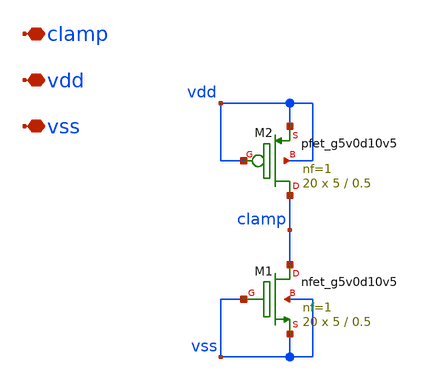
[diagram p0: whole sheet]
** sch_path: images/iic-osic-tools/addons/examples/Open-PMIC-tapeout/xschem/esd_clamp_well.sch
**.subckt esd_clamp_well clamp vdd vss
*.iopin clamp
*.iopin vdd
*.iopin vss
XM1 clamp vss vss vss sky130_fd_pr__nfet_g5v0d10v5 L=0.5 W=5 nf=1 ad='int((nf+1)/2) * W/nf * 0.29' as='int((nf+2)/2) * W/nf * 0.29'
+ pd='2*int((nf+1)/2) * (W/nf + 0.29)' ps='2*int((nf+2)/2) * (W/nf + 0.29)' nrd='0.29 / W' nrs='0.29 / W'
+ sa=0 sb=0 sd=0 mult=20 m=20
XM2 clamp vdd vdd vdd sky130_fd_pr__pfet_g5v0d10v5 L=0.5 W=5 nf=1 ad='int((nf+1)/2) * W/nf * 0.29' as='int((nf+2)/2) * W/nf * 0.29'
+ pd='2*int((nf+1)/2) * (W/nf + 0.29)' ps='2*int((nf+2)/2) * (W/nf + 0.29)' nrd='0.29 / W' nrs='0.29 / W'
+ sa=0 sb=0 sd=0 mult=20 m=20
**.ends
.end
